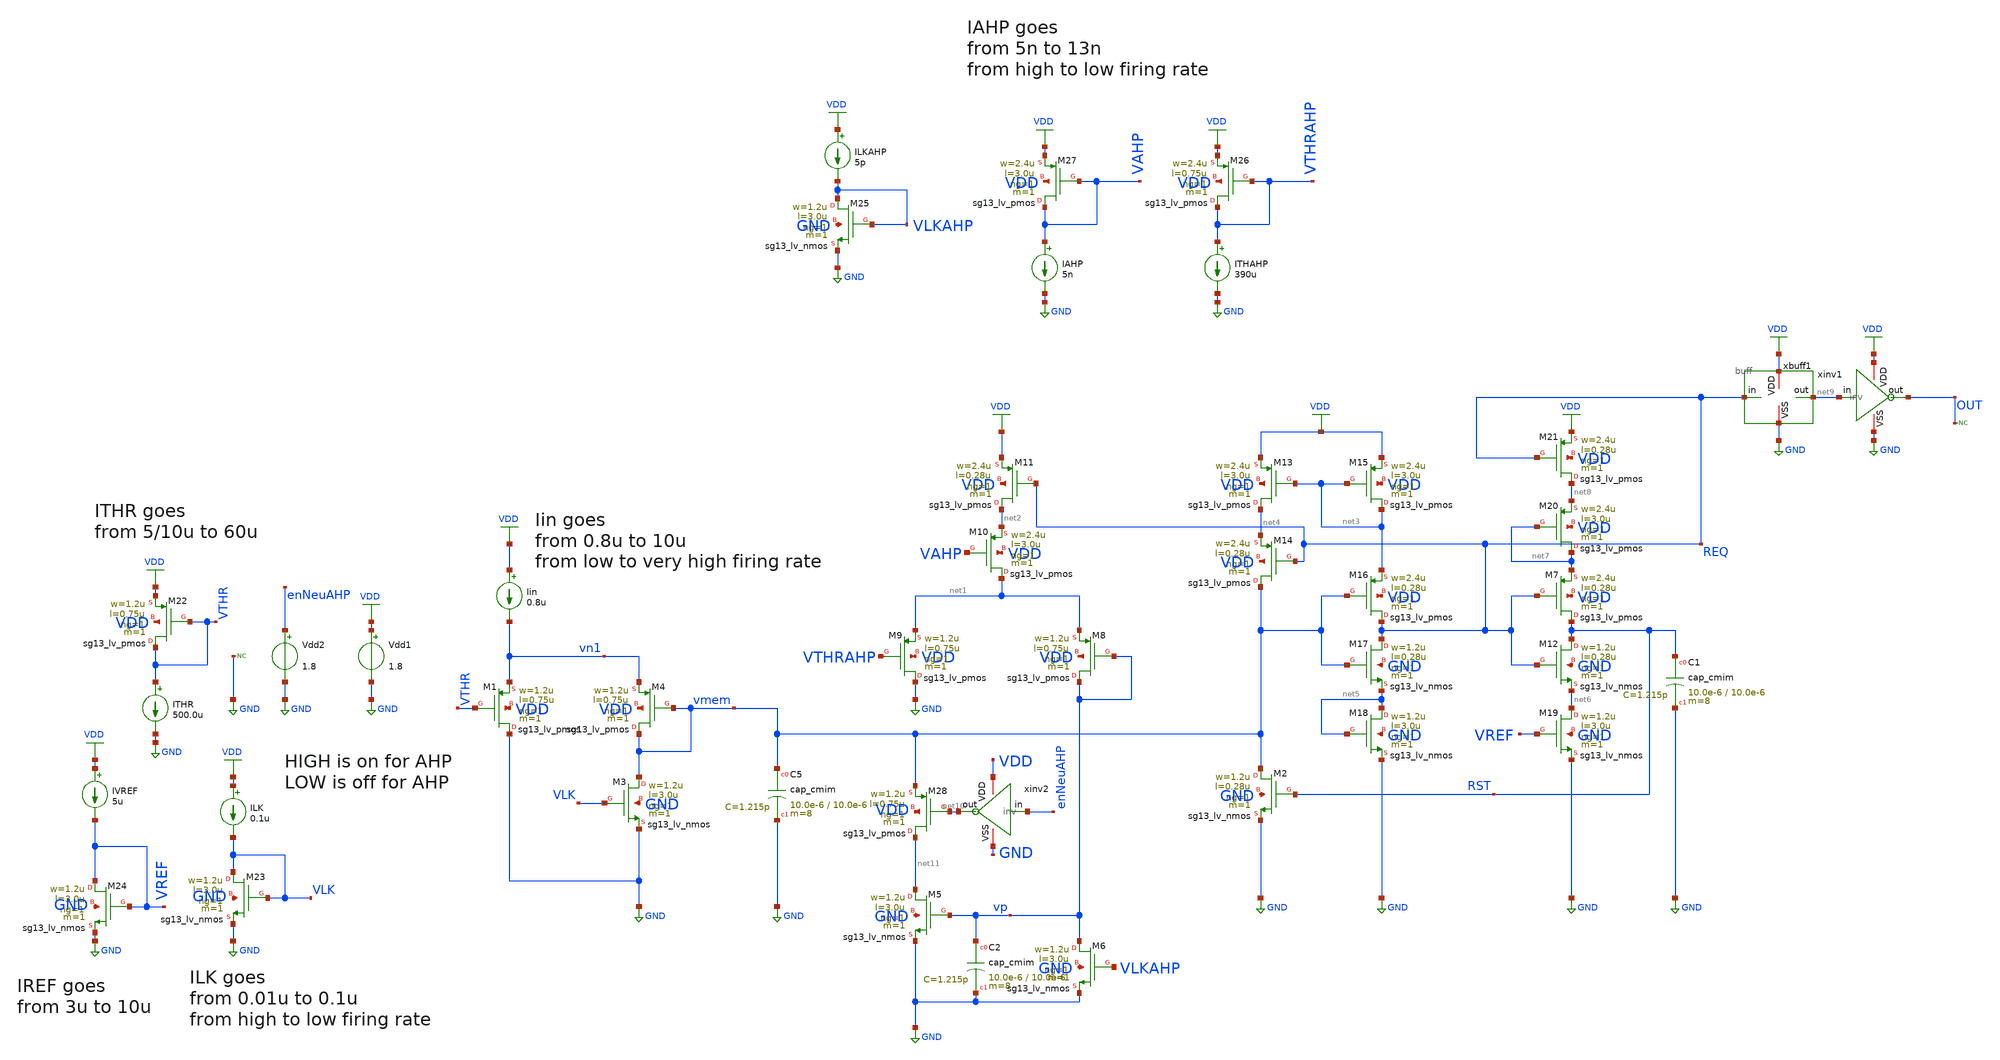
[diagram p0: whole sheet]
** sch_path: blocks/composite/dpi_adexp_neuron/design_data/xschem/neuron2_buff_test_somewhat_working.sch
**.subckt neuron2_buff_test_somewhat_working
Iin VDD vn1 0.8u
XM3 vmem VLK GND GND sg13_lv_nmos w=1.2u l=3.0u ng=1 m=1 mm_ok=1
XM1 GND VTHR vn1 VDD sg13_lv_pmos w=1.2u l=0.75u ng=1 m=1 mm_ok=1
XM4 vmem vmem vn1 VDD sg13_lv_pmos w=1.2u l=0.75u ng=1 m=1 mm_ok=1
XM2 vmem RST GND GND sg13_lv_nmos w=1.2u l=0.28u ng=1 m=1 mm_ok=1
XM5 net11 vp GND GND sg13_lv_nmos w=1.2u l=3.0u ng=1 m=1 mm_ok=1
XM6 vp VLKAHP GND GND sg13_lv_nmos w=1.2u l=3.0u ng=1 m=1 mm_ok=1
XM8 vp vp net1 VDD sg13_lv_pmos w=1.2u l=0.75u ng=1 m=1 mm_ok=1
XM9 GND VTHRAHP net1 VDD sg13_lv_pmos w=1.2u l=0.75u ng=1 m=1 mm_ok=1
XM10 net1 VAHP net2 VDD sg13_lv_pmos w=2.4u l=3.0u ng=1 m=1 mm_ok=1
XM11 net2 REQ VDD VDD sg13_lv_pmos w=2.4u l=0.28u ng=1 m=1 mm_ok=1
XM13 net4 net3 VDD VDD sg13_lv_pmos w=2.4u l=3.0u ng=1 m=1 mm_ok=1
XM14 vmem REQ net4 VDD sg13_lv_pmos w=2.4u l=0.28u ng=1 m=1 mm_ok=1
XM15 net3 net3 VDD VDD sg13_lv_pmos w=2.4u l=3.0u ng=1 m=1 mm_ok=1
XM16 REQ vmem net3 VDD sg13_lv_pmos w=2.4u l=0.28u ng=1 m=1 mm_ok=1
XM17 REQ vmem net5 GND sg13_lv_nmos w=1.2u l=0.28u ng=1 m=1 mm_ok=1
XM18 net5 net5 GND GND sg13_lv_nmos w=1.2u l=3.0u ng=1 m=1 mm_ok=1
XM7 RST REQ net7 VDD sg13_lv_pmos w=2.4u l=0.28u ng=1 m=1 mm_ok=1
XM12 RST REQ net6 GND sg13_lv_nmos w=1.2u l=0.28u ng=1 m=1 mm_ok=1
XM19 net6 VREF GND GND sg13_lv_nmos w=1.2u l=3.0u ng=1 m=1 mm_ok=1
XM20 net7 net7 net8 VDD sg13_lv_pmos w=2.4u l=3.0u ng=1 m=1 mm_ok=1
XM21 net8 REQ VDD VDD sg13_lv_pmos w=2.4u l=0.28u ng=1 m=1 mm_ok=1
xbuff1 VDD REQ net9 GND buff
xinv1 VDD net9 OUT GND inv
Vdd1 VDD GND 1.8
XM23 VLK VLK GND GND sg13_lv_nmos w=1.2u l=3.0u ng=1 m=1 mm_ok=1
ILK VDD VLK 0.1u
XM24 VREF VREF GND GND sg13_lv_nmos w=1.2u l=3.0u ng=1 m=1 mm_ok=1
IVREF VDD VREF 5u
XM25 VLKAHP VLKAHP GND GND sg13_lv_nmos w=1.2u l=3.0u ng=1 m=1 mm_ok=1
ILKAHP VDD VLKAHP 5p
XM26 VTHRAHP VTHRAHP VDD VDD sg13_lv_pmos w=2.4u l=0.75u ng=1 m=1 mm_ok=1
ITHAHP VTHRAHP GND 390u
XM27 VAHP VAHP VDD VDD sg13_lv_pmos w=2.4u l=3.0u ng=1 m=1 mm_ok=1
IAHP VAHP GND 5n
XM22 VTHR VTHR VDD VDD sg13_lv_pmos w=1.2u l=0.75u ng=1 m=1 mm_ok=1
ITHR VTHR GND 500.0u
XC5 vmem GND cap_cmim w=10.0e-6 l=10.0e-6 m=8 mm_ok=1
XC1 RST GND cap_cmim w=10.0e-6 l=10.0e-6 m=8 mm_ok=1
XC2 vp GND cap_cmim w=10.0e-6 l=10.0e-6 m=8 mm_ok=1
xinv2 VDD enNeuAHP net10 GND inv
XM28 net11 net10 vmem VDD sg13_lv_pmos w=1.2u l=0.75u ng=1 m=1 mm_ok=1
Vdd2 enNeuAHP GND 1.8
* noconn OUT
* noconn GND
**** begin user architecture code

.include diodes.lib
.include sg13g2_bondpad.lib



.options savecurrents
.include neuron_buff_test.save
.param temp=27
.control
set wr_singlescale
set noaskquit
*set appendwrite
set hcopypscolor=1

*Save node voltages and device currents if desired
save all

*Baseline operating point at current deck values
op
write tran_neuron.raw

*alter Vdd1 dc 1.7
*alter Vthr dc 0.9
*alter Vlk dc 0.3
*alter vahp1 dc 1.0
tran 500p 2u
write tran_neuron.raw
*Example plots (uncomment inside ngspice if you want autoplots)
plot vmem vn1 Vthr Vlk
plot vmem out
.endc





.lib cornerMOSlv.lib mos_tt
.lib cornerMOShv.lib mos_tt
.lib cornerHBT.lib hbt_typ
.lib cornerRES.lib res_typ
.lib cornerCAP.lib cap_typ



**** end user architecture code
**.ends
.GLOBAL GND
.GLOBAL VDD
.end
